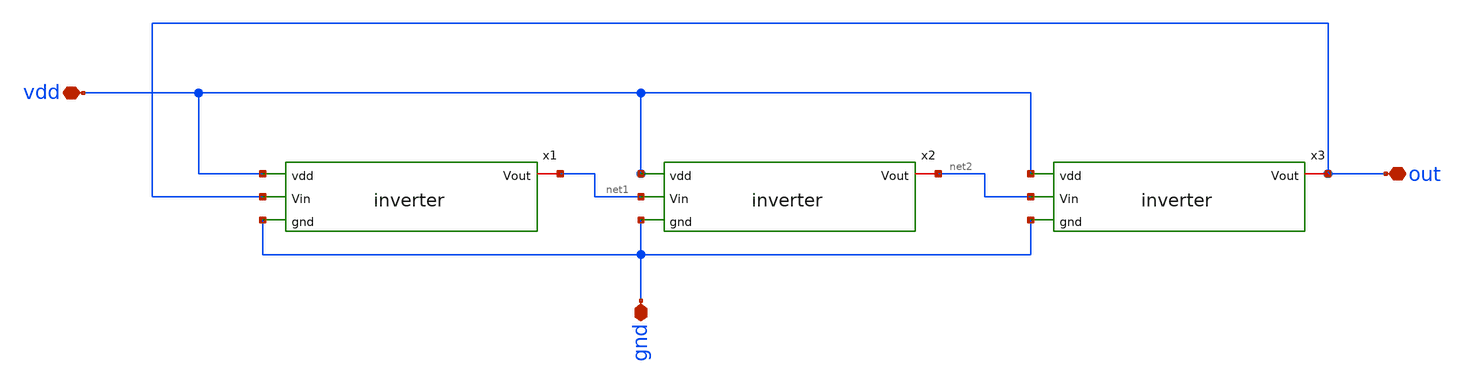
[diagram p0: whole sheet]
** sch_path: ringosci/ringosci.sch
**.subckt ringosci out vdd gnd
*.iopin out
*.iopin vdd
*.iopin gnd
x1 vdd net1 out gnd inverter
x2 vdd net2 net1 gnd inverter
x3 vdd out net2 gnd inverter
**.ends
.end
